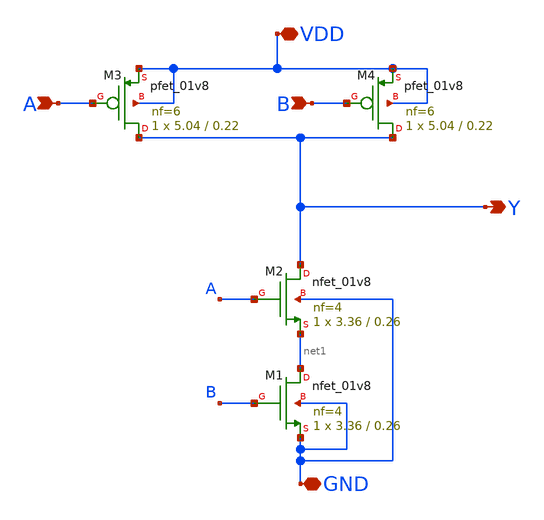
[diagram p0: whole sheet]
** sch_path: cells/NAND2X4/schematic/nand2x4.sch
**.subckt nand2x4 A B VDD GND Y
*.ipin A
*.ipin B
*.iopin VDD
*.iopin GND
*.opin Y
XM2 Y A net1 GND sky130_fd_pr__nfet_01v8 L=0.26 W=3.36 nf=4 ad='int((4 + 1)/2) * 3.36 / 4 * 0.29' as='int((4 + 2)/2) * 3.36 / 4 * 0.29'
+ pd='2*int((4 + 1)/2) * (3.36 / 4 + 0.29)' ps='2*int((4 + 2)/2) * (3.36 / 4 + 0.29)' nrd='0.29 / 3.36 '
+ nrs='0.29 / 3.36 ' sa=0 sb=0 sd=0 mult=1 m=1
XM3 Y A VDD VDD sky130_fd_pr__pfet_01v8 L=0.22 W=5.04 nf=6 ad='int((6 + 1)/2) * 5.04 / 6 * 0.29' as='int((6 + 2)/2) * 5.04 / 6 * 0.29'
+ pd='2*int((6 + 1)/2) * (5.04 / 6 + 0.29)' ps='2*int((6 + 2)/2) * (5.04 / 6 + 0.29)' nrd='0.29 / 5.04 '
+ nrs='0.29 / 5.04 ' sa=0 sb=0 sd=0 mult=1 m=1
XM4 Y B VDD VDD sky130_fd_pr__pfet_01v8 L=0.22 W=5.04 nf=6 ad='int((6 + 1)/2) * 5.04 / 6 * 0.29' as='int((6 + 2)/2) * 5.04 / 6 * 0.29'
+ pd='2*int((6 + 1)/2) * (5.04 / 6 + 0.29)' ps='2*int((6 + 2)/2) * (5.04 / 6 + 0.29)' nrd='0.29 / 5.04 '
+ nrs='0.29 / 5.04 ' sa=0 sb=0 sd=0 mult=1 m=1
XM1 net1 B GND GND sky130_fd_pr__nfet_01v8 L=0.26 W=3.36 nf=4 ad='int((4 + 1)/2) * 3.36 / 4 * 0.29' as='int((4 + 2)/2) * 3.36 / 4 * 0.29'
+ pd='2*int((4 + 1)/2) * (3.36 / 4 + 0.29)' ps='2*int((4 + 2)/2) * (3.36 / 4 + 0.29)' nrd='0.29 / 3.36 '
+ nrs='0.29 / 3.36 ' sa=0 sb=0 sd=0 mult=1 m=1
**.ends
.end
